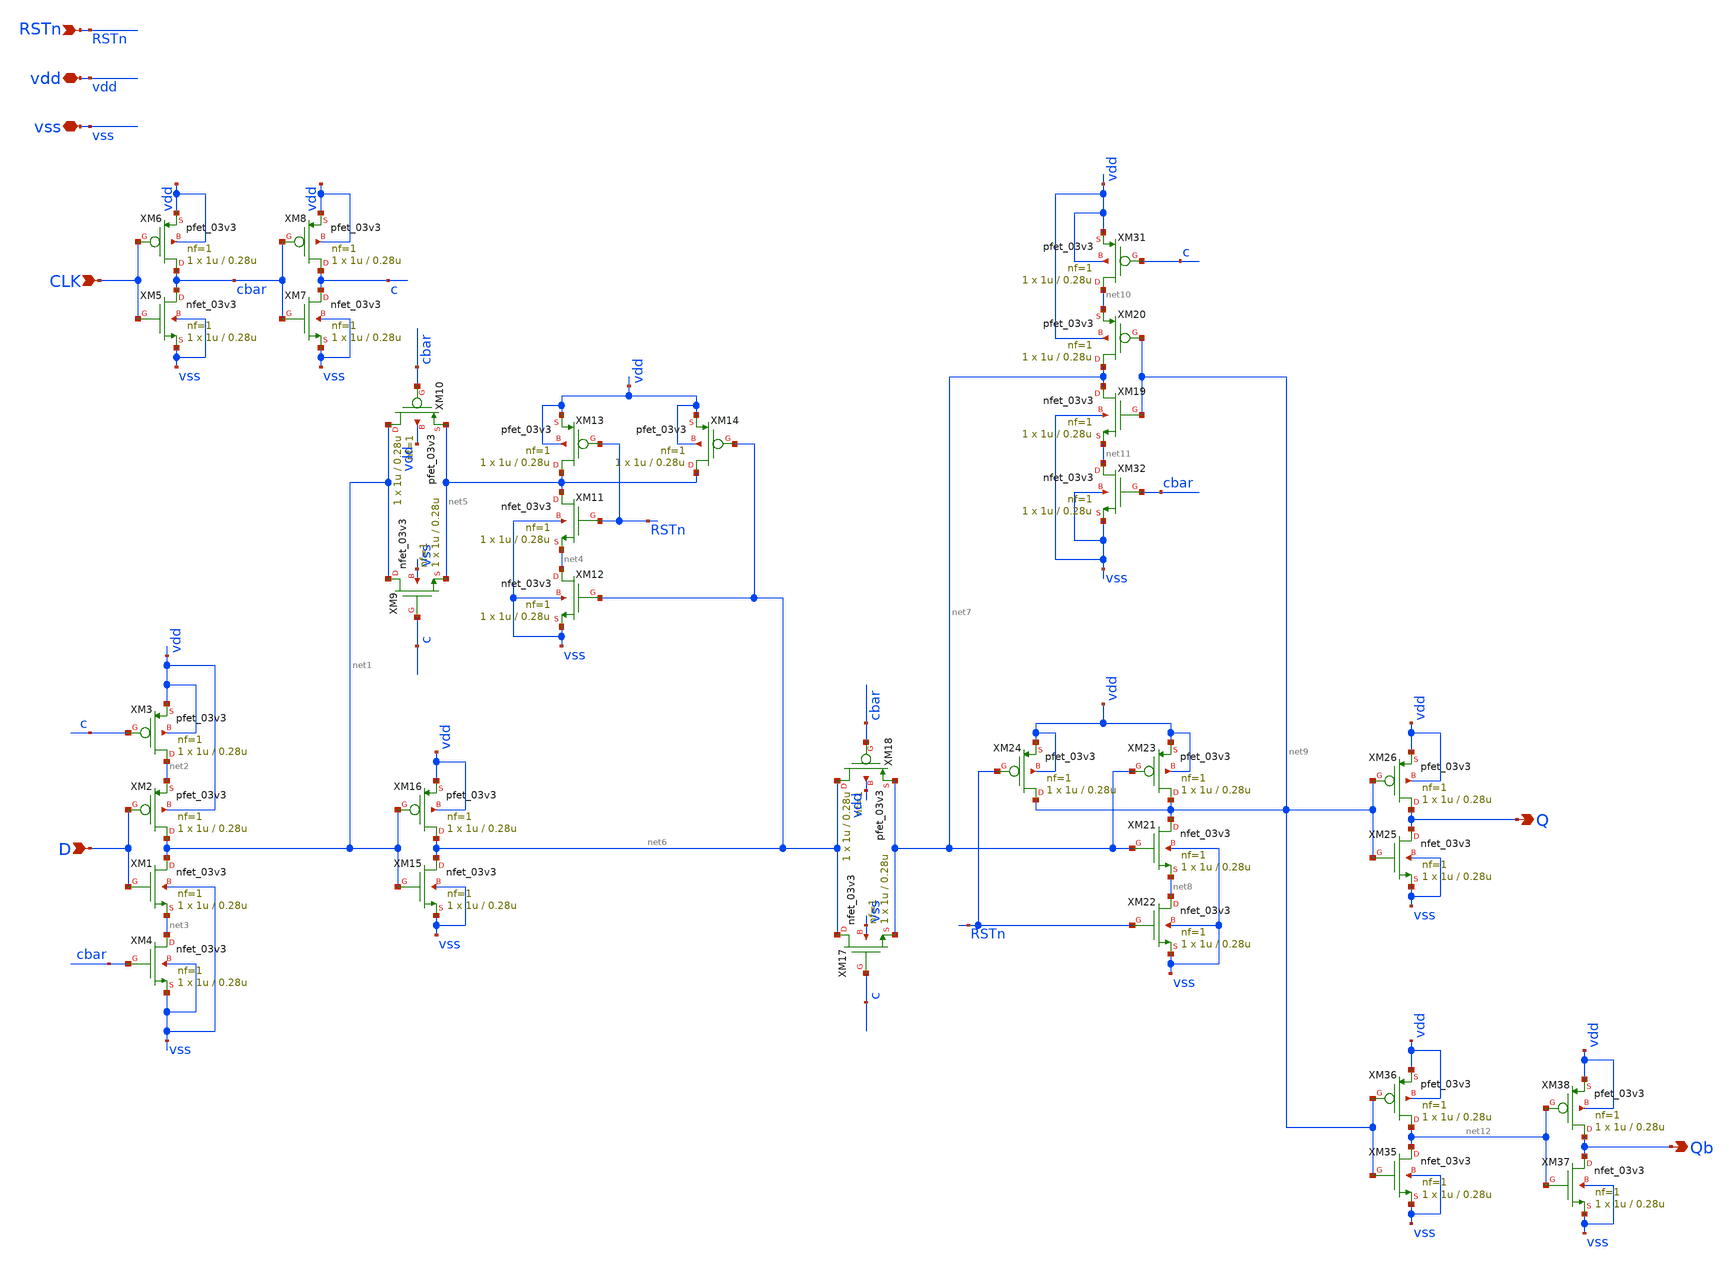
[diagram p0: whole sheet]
** sch_path: schematics/PC/DFF/DFF.sch
**.subckt DFF D CLK RSTn Q vdd vss Qb
*.ipin D
*.ipin CLK
*.ipin RSTn
*.opin Q
*.iopin vdd
*.iopin vss
*.opin Qb
XM1 net1 D net3 vss nfet_03v3 L=0.28u W=1u nf=1 ad='int((nf+1)/2) * W/nf * 0.18u' as='int((nf+2)/2) * W/nf * 0.18u'
+ pd='2*int((nf+1)/2) * (W/nf + 0.18u)' ps='2*int((nf+2)/2) * (W/nf + 0.18u)' nrd='0.18u / W' nrs='0.18u / W'
+ sa=0 sb=0 sd=0 m=1
XM2 net1 D net2 vdd pfet_03v3 L=0.28u W=1u nf=1 ad='int((nf+1)/2) * W/nf * 0.18u' as='int((nf+2)/2) * W/nf * 0.18u'
+ pd='2*int((nf+1)/2) * (W/nf + 0.18u)' ps='2*int((nf+2)/2) * (W/nf + 0.18u)' nrd='0.18u / W' nrs='0.18u / W'
+ sa=0 sb=0 sd=0 m=1
XM3 net2 c vdd vdd pfet_03v3 L=0.28u W=1u nf=1 ad='int((nf+1)/2) * W/nf * 0.18u' as='int((nf+2)/2) * W/nf * 0.18u'
+ pd='2*int((nf+1)/2) * (W/nf + 0.18u)' ps='2*int((nf+2)/2) * (W/nf + 0.18u)' nrd='0.18u / W' nrs='0.18u / W'
+ sa=0 sb=0 sd=0 m=1
XM4 net3 cbar vss vss nfet_03v3 L=0.28u W=1u nf=1 ad='int((nf+1)/2) * W/nf * 0.18u' as='int((nf+2)/2) * W/nf * 0.18u'
+ pd='2*int((nf+1)/2) * (W/nf + 0.18u)' ps='2*int((nf+2)/2) * (W/nf + 0.18u)' nrd='0.18u / W' nrs='0.18u / W'
+ sa=0 sb=0 sd=0 m=1
XM5 cbar CLK vss vss nfet_03v3 L=0.28u W=1u nf=1 ad='int((nf+1)/2) * W/nf * 0.18u' as='int((nf+2)/2) * W/nf * 0.18u'
+ pd='2*int((nf+1)/2) * (W/nf + 0.18u)' ps='2*int((nf+2)/2) * (W/nf + 0.18u)' nrd='0.18u / W' nrs='0.18u / W'
+ sa=0 sb=0 sd=0 m=1
XM6 cbar CLK vdd vdd pfet_03v3 L=0.28u W=1u nf=1 ad='int((nf+1)/2) * W/nf * 0.18u' as='int((nf+2)/2) * W/nf * 0.18u'
+ pd='2*int((nf+1)/2) * (W/nf + 0.18u)' ps='2*int((nf+2)/2) * (W/nf + 0.18u)' nrd='0.18u / W' nrs='0.18u / W'
+ sa=0 sb=0 sd=0 m=1
XM7 c cbar vss vss nfet_03v3 L=0.28u W=1u nf=1 ad='int((nf+1)/2) * W/nf * 0.18u' as='int((nf+2)/2) * W/nf * 0.18u'
+ pd='2*int((nf+1)/2) * (W/nf + 0.18u)' ps='2*int((nf+2)/2) * (W/nf + 0.18u)' nrd='0.18u / W' nrs='0.18u / W'
+ sa=0 sb=0 sd=0 m=1
XM8 c cbar vdd vdd pfet_03v3 L=0.28u W=1u nf=1 ad='int((nf+1)/2) * W/nf * 0.18u' as='int((nf+2)/2) * W/nf * 0.18u'
+ pd='2*int((nf+1)/2) * (W/nf + 0.18u)' ps='2*int((nf+2)/2) * (W/nf + 0.18u)' nrd='0.18u / W' nrs='0.18u / W'
+ sa=0 sb=0 sd=0 m=1
XM11 net5 RSTn net4 vss nfet_03v3 L=0.28u W=1u nf=1 ad='int((nf+1)/2) * W/nf * 0.18u' as='int((nf+2)/2) * W/nf * 0.18u'
+ pd='2*int((nf+1)/2) * (W/nf + 0.18u)' ps='2*int((nf+2)/2) * (W/nf + 0.18u)' nrd='0.18u / W' nrs='0.18u / W'
+ sa=0 sb=0 sd=0 m=1
XM12 net4 net6 vss vss nfet_03v3 L=0.28u W=1u nf=1 ad='int((nf+1)/2) * W/nf * 0.18u' as='int((nf+2)/2) * W/nf * 0.18u'
+ pd='2*int((nf+1)/2) * (W/nf + 0.18u)' ps='2*int((nf+2)/2) * (W/nf + 0.18u)' nrd='0.18u / W' nrs='0.18u / W'
+ sa=0 sb=0 sd=0 m=1
XM13 net5 RSTn vdd vdd pfet_03v3 L=0.28u W=1u nf=1 ad='int((nf+1)/2) * W/nf * 0.18u' as='int((nf+2)/2) * W/nf * 0.18u'
+ pd='2*int((nf+1)/2) * (W/nf + 0.18u)' ps='2*int((nf+2)/2) * (W/nf + 0.18u)' nrd='0.18u / W' nrs='0.18u / W'
+ sa=0 sb=0 sd=0 m=1
XM14 net5 net6 vdd vdd pfet_03v3 L=0.28u W=1u nf=1 ad='int((nf+1)/2) * W/nf * 0.18u' as='int((nf+2)/2) * W/nf * 0.18u'
+ pd='2*int((nf+1)/2) * (W/nf + 0.18u)' ps='2*int((nf+2)/2) * (W/nf + 0.18u)' nrd='0.18u / W' nrs='0.18u / W'
+ sa=0 sb=0 sd=0 m=1
XM15 net6 net1 vss vss nfet_03v3 L=0.28u W=1u nf=1 ad='int((nf+1)/2) * W/nf * 0.18u' as='int((nf+2)/2) * W/nf * 0.18u'
+ pd='2*int((nf+1)/2) * (W/nf + 0.18u)' ps='2*int((nf+2)/2) * (W/nf + 0.18u)' nrd='0.18u / W' nrs='0.18u / W'
+ sa=0 sb=0 sd=0 m=1
XM16 net6 net1 vdd vdd pfet_03v3 L=0.28u W=1u nf=1 ad='int((nf+1)/2) * W/nf * 0.18u' as='int((nf+2)/2) * W/nf * 0.18u'
+ pd='2*int((nf+1)/2) * (W/nf + 0.18u)' ps='2*int((nf+2)/2) * (W/nf + 0.18u)' nrd='0.18u / W' nrs='0.18u / W'
+ sa=0 sb=0 sd=0 m=1
XM21 net9 net7 net8 vss nfet_03v3 L=0.28u W=1u nf=1 ad='int((nf+1)/2) * W/nf * 0.18u' as='int((nf+2)/2) * W/nf * 0.18u'
+ pd='2*int((nf+1)/2) * (W/nf + 0.18u)' ps='2*int((nf+2)/2) * (W/nf + 0.18u)' nrd='0.18u / W' nrs='0.18u / W'
+ sa=0 sb=0 sd=0 m=1
XM22 net8 RSTn vss vss nfet_03v3 L=0.28u W=1u nf=1 ad='int((nf+1)/2) * W/nf * 0.18u' as='int((nf+2)/2) * W/nf * 0.18u'
+ pd='2*int((nf+1)/2) * (W/nf + 0.18u)' ps='2*int((nf+2)/2) * (W/nf + 0.18u)' nrd='0.18u / W' nrs='0.18u / W'
+ sa=0 sb=0 sd=0 m=1
XM23 net9 net7 vdd vdd pfet_03v3 L=0.28u W=1u nf=1 ad='int((nf+1)/2) * W/nf * 0.18u' as='int((nf+2)/2) * W/nf * 0.18u'
+ pd='2*int((nf+1)/2) * (W/nf + 0.18u)' ps='2*int((nf+2)/2) * (W/nf + 0.18u)' nrd='0.18u / W' nrs='0.18u / W'
+ sa=0 sb=0 sd=0 m=1
XM24 net9 RSTn vdd vdd pfet_03v3 L=0.28u W=1u nf=1 ad='int((nf+1)/2) * W/nf * 0.18u' as='int((nf+2)/2) * W/nf * 0.18u'
+ pd='2*int((nf+1)/2) * (W/nf + 0.18u)' ps='2*int((nf+2)/2) * (W/nf + 0.18u)' nrd='0.18u / W' nrs='0.18u / W'
+ sa=0 sb=0 sd=0 m=1
XM25 Q net9 vss vss nfet_03v3 L=0.28u W=1u nf=1 ad='int((nf+1)/2) * W/nf * 0.18u' as='int((nf+2)/2) * W/nf * 0.18u'
+ pd='2*int((nf+1)/2) * (W/nf + 0.18u)' ps='2*int((nf+2)/2) * (W/nf + 0.18u)' nrd='0.18u / W' nrs='0.18u / W'
+ sa=0 sb=0 sd=0 m=1
XM26 Q net9 vdd vdd pfet_03v3 L=0.28u W=1u nf=1 ad='int((nf+1)/2) * W/nf * 0.18u' as='int((nf+2)/2) * W/nf * 0.18u'
+ pd='2*int((nf+1)/2) * (W/nf + 0.18u)' ps='2*int((nf+2)/2) * (W/nf + 0.18u)' nrd='0.18u / W' nrs='0.18u / W'
+ sa=0 sb=0 sd=0 m=1
XM19 net7 net9 net11 vss nfet_03v3 L=0.28u W=1u nf=1 ad='int((nf+1)/2) * W/nf * 0.18u' as='int((nf+2)/2) * W/nf * 0.18u'
+ pd='2*int((nf+1)/2) * (W/nf + 0.18u)' ps='2*int((nf+2)/2) * (W/nf + 0.18u)' nrd='0.18u / W' nrs='0.18u / W'
+ sa=0 sb=0 sd=0 m=1
XM20 net7 net9 net10 vdd pfet_03v3 L=0.28u W=1u nf=1 ad='int((nf+1)/2) * W/nf * 0.18u' as='int((nf+2)/2) * W/nf * 0.18u'
+ pd='2*int((nf+1)/2) * (W/nf + 0.18u)' ps='2*int((nf+2)/2) * (W/nf + 0.18u)' nrd='0.18u / W' nrs='0.18u / W'
+ sa=0 sb=0 sd=0 m=1
XM31 net10 c vdd vdd pfet_03v3 L=0.28u W=1u nf=1 ad='int((nf+1)/2) * W/nf * 0.18u' as='int((nf+2)/2) * W/nf * 0.18u'
+ pd='2*int((nf+1)/2) * (W/nf + 0.18u)' ps='2*int((nf+2)/2) * (W/nf + 0.18u)' nrd='0.18u / W' nrs='0.18u / W'
+ sa=0 sb=0 sd=0 m=1
XM32 net11 cbar vss vss nfet_03v3 L=0.28u W=1u nf=1 ad='int((nf+1)/2) * W/nf * 0.18u' as='int((nf+2)/2) * W/nf * 0.18u'
+ pd='2*int((nf+1)/2) * (W/nf + 0.18u)' ps='2*int((nf+2)/2) * (W/nf + 0.18u)' nrd='0.18u / W' nrs='0.18u / W'
+ sa=0 sb=0 sd=0 m=1
XM35 net12 net9 vss vss nfet_03v3 L=0.28u W=1u nf=1 ad='int((nf+1)/2) * W/nf * 0.18u' as='int((nf+2)/2) * W/nf * 0.18u'
+ pd='2*int((nf+1)/2) * (W/nf + 0.18u)' ps='2*int((nf+2)/2) * (W/nf + 0.18u)' nrd='0.18u / W' nrs='0.18u / W'
+ sa=0 sb=0 sd=0 m=1
XM36 net12 net9 vdd vdd pfet_03v3 L=0.28u W=1u nf=1 ad='int((nf+1)/2) * W/nf * 0.18u' as='int((nf+2)/2) * W/nf * 0.18u'
+ pd='2*int((nf+1)/2) * (W/nf + 0.18u)' ps='2*int((nf+2)/2) * (W/nf + 0.18u)' nrd='0.18u / W' nrs='0.18u / W'
+ sa=0 sb=0 sd=0 m=1
XM37 Qb net12 vss vss nfet_03v3 L=0.28u W=1u nf=1 ad='int((nf+1)/2) * W/nf * 0.18u' as='int((nf+2)/2) * W/nf * 0.18u'
+ pd='2*int((nf+1)/2) * (W/nf + 0.18u)' ps='2*int((nf+2)/2) * (W/nf + 0.18u)' nrd='0.18u / W' nrs='0.18u / W'
+ sa=0 sb=0 sd=0 m=1
XM38 Qb net12 vdd vdd pfet_03v3 L=0.28u W=1u nf=1 ad='int((nf+1)/2) * W/nf * 0.18u' as='int((nf+2)/2) * W/nf * 0.18u'
+ pd='2*int((nf+1)/2) * (W/nf + 0.18u)' ps='2*int((nf+2)/2) * (W/nf + 0.18u)' nrd='0.18u / W' nrs='0.18u / W'
+ sa=0 sb=0 sd=0 m=1
XM9 net1 c net5 vss nfet_03v3 L=0.28u W=1u nf=1 ad='int((nf+1)/2) * W/nf * 0.18u' as='int((nf+2)/2) * W/nf * 0.18u'
+ pd='2*int((nf+1)/2) * (W/nf + 0.18u)' ps='2*int((nf+2)/2) * (W/nf + 0.18u)' nrd='0.18u / W' nrs='0.18u / W'
+ sa=0 sb=0 sd=0 m=1
XM10 net1 cbar net5 vdd pfet_03v3 L=0.28u W=1u nf=1 ad='int((nf+1)/2) * W/nf * 0.18u' as='int((nf+2)/2) * W/nf * 0.18u'
+ pd='2*int((nf+1)/2) * (W/nf + 0.18u)' ps='2*int((nf+2)/2) * (W/nf + 0.18u)' nrd='0.18u / W' nrs='0.18u / W'
+ sa=0 sb=0 sd=0 m=1
XM17 net6 c net7 vss nfet_03v3 L=0.28u W=1u nf=1 ad='int((nf+1)/2) * W/nf * 0.18u' as='int((nf+2)/2) * W/nf * 0.18u'
+ pd='2*int((nf+1)/2) * (W/nf + 0.18u)' ps='2*int((nf+2)/2) * (W/nf + 0.18u)' nrd='0.18u / W' nrs='0.18u / W'
+ sa=0 sb=0 sd=0 m=1
XM18 net6 cbar net7 vdd pfet_03v3 L=0.28u W=1u nf=1 ad='int((nf+1)/2) * W/nf * 0.18u' as='int((nf+2)/2) * W/nf * 0.18u'
+ pd='2*int((nf+1)/2) * (W/nf + 0.18u)' ps='2*int((nf+2)/2) * (W/nf + 0.18u)' nrd='0.18u / W' nrs='0.18u / W'
+ sa=0 sb=0 sd=0 m=1
**.ends
.end
